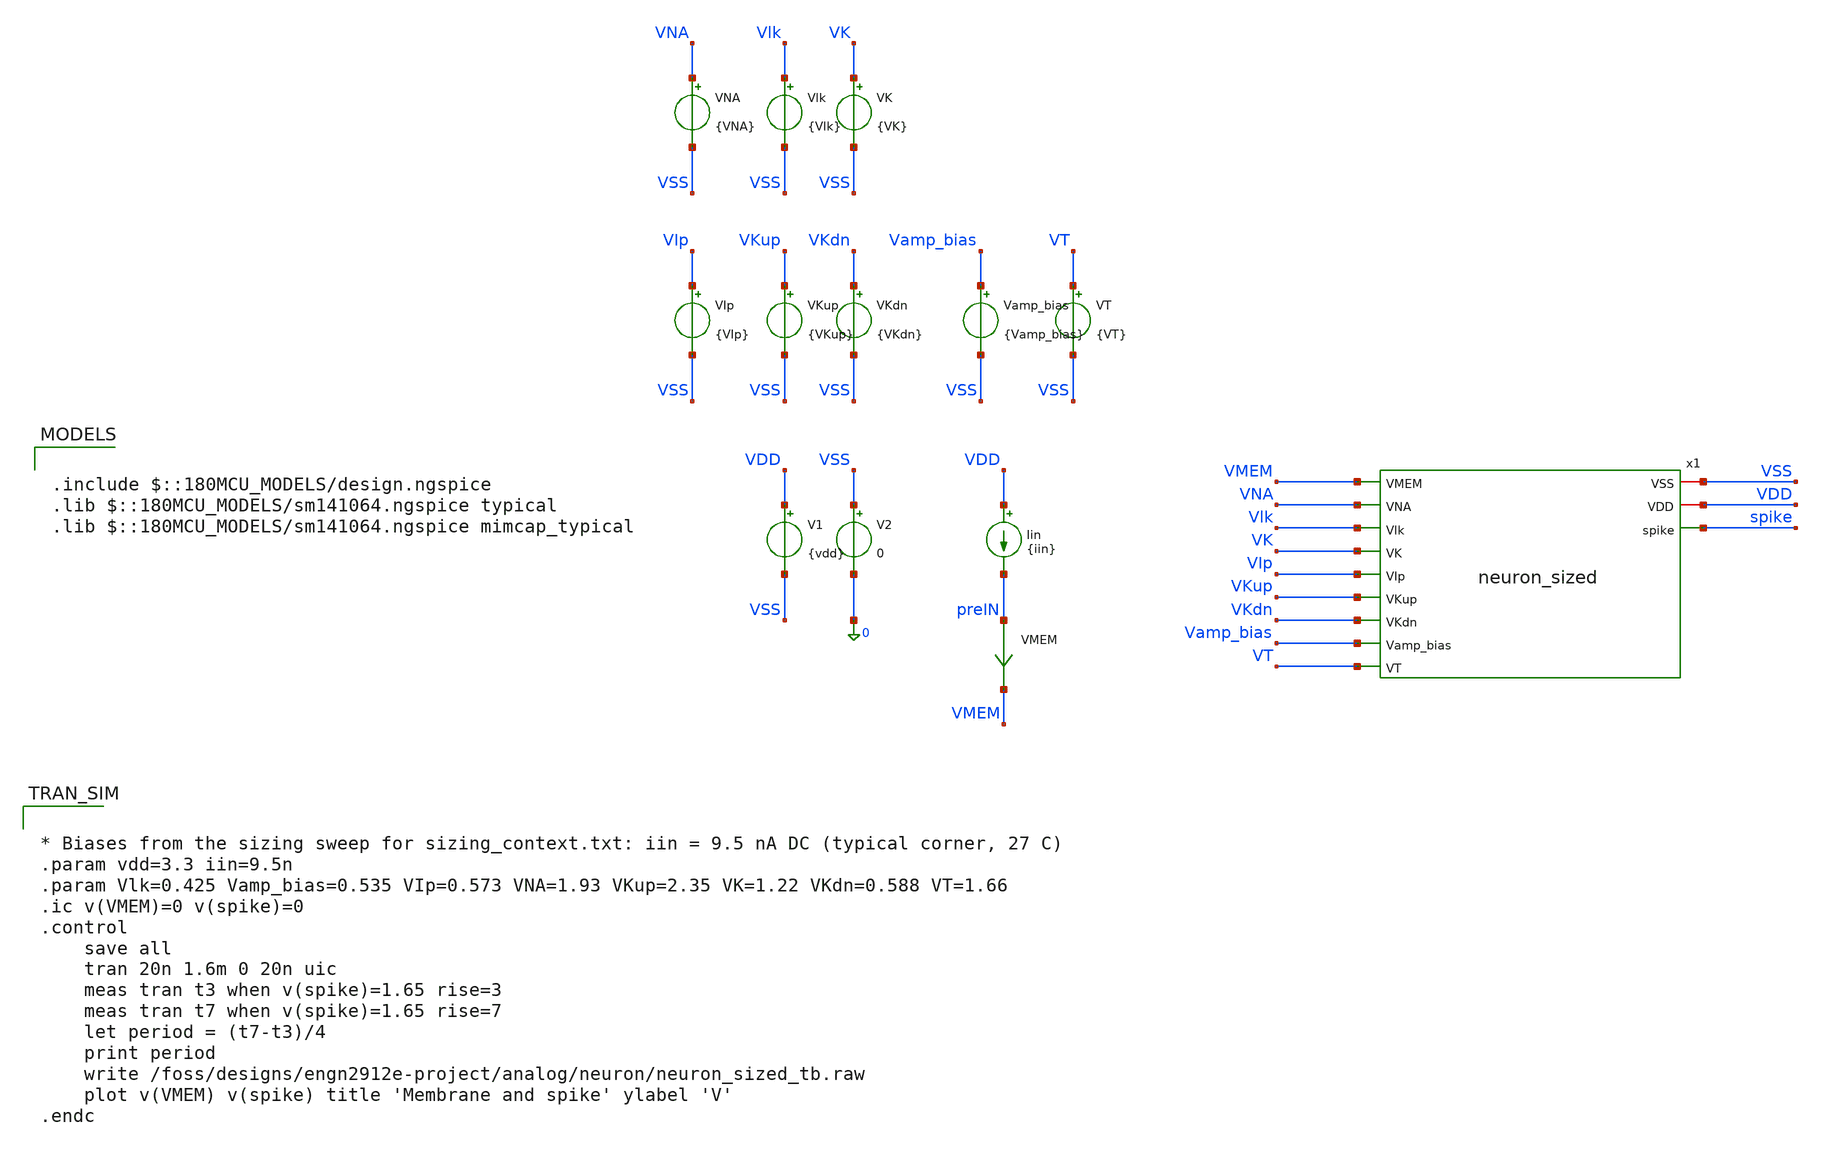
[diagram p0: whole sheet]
** sch_path: analog/neuron/neuron_sized_testbench.sch
**.subckt neuron_sized_testbench
V1 VDD VSS {vdd}
V2 VSS 0 0
Iin VDD preIN {iin}
VMEM preIN VMEM 0
.save i(vmem)
x1 VSS VDD VMEM VNA Vlk VK VIp VKup VKdn Vamp_bias VT spike neuron_sized
Vlk Vlk VSS {Vlk}
VK VK VSS {VK}
VNA VNA VSS {VNA}
VKup VKup VSS {VKup}
VKdn VKdn VSS {VKdn}
VIp VIp VSS {VIp}
VT VT VSS {VT}
Vamp_bias Vamp_bias VSS {Vamp_bias}
**** begin user architecture code

.include $::180MCU_MODELS/design.ngspice
.lib $::180MCU_MODELS/sm141064.ngspice typical
.lib $::180MCU_MODELS/sm141064.ngspice mimcap_typical



* Biases from the sizing sweep for sizing_context.txt: iin = 9.5 nA DC (typical corner, 27 C)
.param vdd=3.3 iin=9.5n
.param Vlk=0.425 Vamp_bias=0.535 VIp=0.573 VNA=1.93 VKup=2.35 VK=1.22 VKdn=0.588 VT=1.66
.ic v(VMEM)=0 v(spike)=0
.control
	save all
	tran 20n 1.6m 0 20n uic
	meas tran t3 when v(spike)=1.65 rise=3
	meas tran t7 when v(spike)=1.65 rise=7
	let period = (t7-t3)/4
	print period
	write /foss/designs/engn2912e-project/analog/neuron/neuron_sized_tb.raw
	plot v(VMEM) v(spike) title 'Membrane and spike' ylabel 'V'
.endc


**** end user architecture code
**.ends
.end
